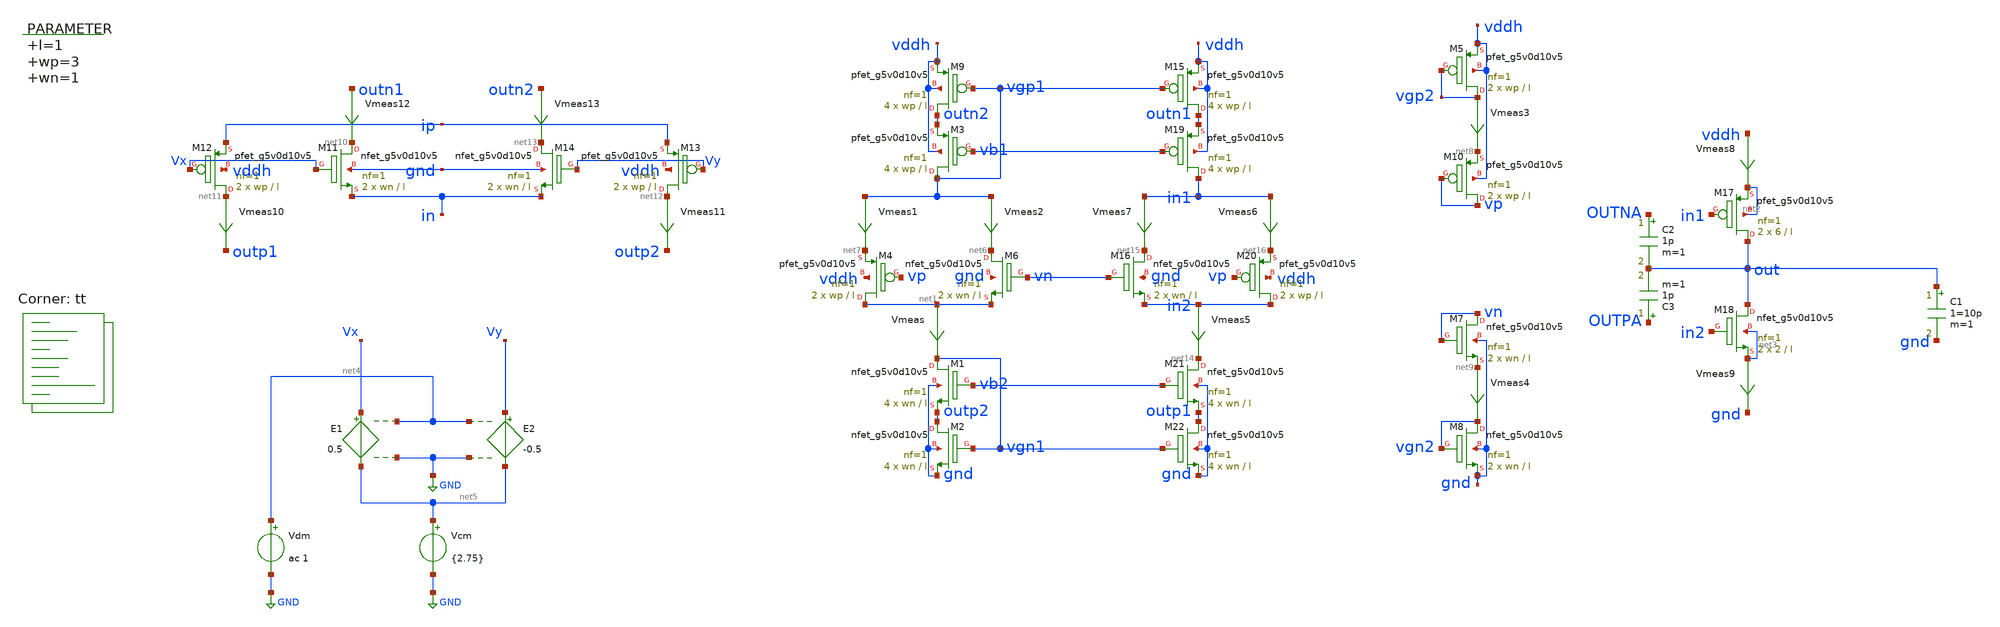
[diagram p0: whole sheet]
** sch_path: xschem/op_amp_output_stage.sch
**.subckt op_amp_output_stage
Vmeas net1 vgn1 0
.save i(vmeas)
XM9 outn2 vgp1 vddh vddh sky130_fd_pr__pfet_g5v0d10v5 L=l W=wp nf=1 ad='int((nf+1)/2) * W/nf * 0.29'
+ as='int((nf+2)/2) * W/nf * 0.29' pd='2*int((nf+1)/2) * (W/nf + 0.29)' ps='2*int((nf+2)/2) * (W/nf + 0.29)'
+ nrd='0.29 / W' nrs='0.29 / W' sa=0 sb=0 sd=0 mult=4 m=4
XM6 net6 vn net1 gnd sky130_fd_pr__nfet_g5v0d10v5 L=l W=wn nf=1 ad='int((nf+1)/2) * W/nf * 0.29' as='int((nf+2)/2) * W/nf * 0.29'
+ pd='2*int((nf+1)/2) * (W/nf + 0.29)' ps='2*int((nf+2)/2) * (W/nf + 0.29)' nrd='0.29 / W' nrs='0.29 / W'
+ sa=0 sb=0 sd=0 mult=2 m=2
Vmeas1 vgp1 net7 0
.save i(vmeas1)
Vmeas2 vgp1 net6 0
.save i(vmeas2)
Vmeas3 vgp2 net8 0
.save i(vmeas3)
Vmeas4 net9 vgn2 0
.save i(vmeas4)
XM3 vgp1 vb1 outn2 vddh sky130_fd_pr__pfet_g5v0d10v5 L=l W=wp nf=1 ad='int((nf+1)/2) * W/nf * 0.29' as='int((nf+2)/2) * W/nf * 0.29'
+ pd='2*int((nf+1)/2) * (W/nf + 0.29)' ps='2*int((nf+2)/2) * (W/nf + 0.29)' nrd='0.29 / W' nrs='0.29 / W'
+ sa=0 sb=0 sd=0 mult=4 m=4
XM4 net1 vp net7 vddh sky130_fd_pr__pfet_g5v0d10v5 L=l W=wp nf=1 ad='int((nf+1)/2) * W/nf * 0.29' as='int((nf+2)/2) * W/nf * 0.29'
+ pd='2*int((nf+1)/2) * (W/nf + 0.29)' ps='2*int((nf+2)/2) * (W/nf + 0.29)' nrd='0.29 / W' nrs='0.29 / W'
+ sa=0 sb=0 sd=0 mult=2 m=2
XM5 vgp2 vgp2 vddh vddh sky130_fd_pr__pfet_g5v0d10v5 L=l W=wp nf=1 ad='int((nf+1)/2) * W/nf * 0.29' as='int((nf+2)/2) * W/nf * 0.29'
+ pd='2*int((nf+1)/2) * (W/nf + 0.29)' ps='2*int((nf+2)/2) * (W/nf + 0.29)' nrd='0.29 / W' nrs='0.29 / W'
+ sa=0 sb=0 sd=0 mult=2 m=2
XM10 vp vp net8 vddh sky130_fd_pr__pfet_g5v0d10v5 L=l W=wp nf=1 ad='int((nf+1)/2) * W/nf * 0.29' as='int((nf+2)/2) * W/nf * 0.29'
+ pd='2*int((nf+1)/2) * (W/nf + 0.29)' ps='2*int((nf+2)/2) * (W/nf + 0.29)' nrd='0.29 / W' nrs='0.29 / W'
+ sa=0 sb=0 sd=0 mult=2 m=2
XM1 vgn1 vb2 outp2 gnd sky130_fd_pr__nfet_g5v0d10v5 L=l W=wn nf=1 ad='int((nf+1)/2) * W/nf * 0.29' as='int((nf+2)/2) * W/nf * 0.29'
+ pd='2*int((nf+1)/2) * (W/nf + 0.29)' ps='2*int((nf+2)/2) * (W/nf + 0.29)' nrd='0.29 / W' nrs='0.29 / W'
+ sa=0 sb=0 sd=0 mult=4 m=4
XM2 outp2 vgn1 gnd gnd sky130_fd_pr__nfet_g5v0d10v5 L=l W=wn nf=1 ad='int((nf+1)/2) * W/nf * 0.29' as='int((nf+2)/2) * W/nf * 0.29'
+ pd='2*int((nf+1)/2) * (W/nf + 0.29)' ps='2*int((nf+2)/2) * (W/nf + 0.29)' nrd='0.29 / W' nrs='0.29 / W'
+ sa=0 sb=0 sd=0 mult=4 m=4
XM7 vn vn net9 gnd sky130_fd_pr__nfet_g5v0d10v5 L=l W=wn nf=1 ad='int((nf+1)/2) * W/nf * 0.29' as='int((nf+2)/2) * W/nf * 0.29'
+ pd='2*int((nf+1)/2) * (W/nf + 0.29)' ps='2*int((nf+2)/2) * (W/nf + 0.29)' nrd='0.29 / W' nrs='0.29 / W'
+ sa=0 sb=0 sd=0 mult=2 m=2
XM8 vgn2 vgn2 gnd gnd sky130_fd_pr__nfet_g5v0d10v5 L=l W=wn nf=1 ad='int((nf+1)/2) * W/nf * 0.29' as='int((nf+2)/2) * W/nf * 0.29'
+ pd='2*int((nf+1)/2) * (W/nf + 0.29)' ps='2*int((nf+2)/2) * (W/nf + 0.29)' nrd='0.29 / W' nrs='0.29 / W'
+ sa=0 sb=0 sd=0 mult=2 m=2
.param l=1 wp=3 wn=1
XM17 out in1 net2 net2 sky130_fd_pr__pfet_g5v0d10v5 L=l W=6 nf=1 ad='int((nf+1)/2) * W/nf * 0.29' as='int((nf+2)/2) * W/nf * 0.29'
+ pd='2*int((nf+1)/2) * (W/nf + 0.29)' ps='2*int((nf+2)/2) * (W/nf + 0.29)' nrd='0.29 / W' nrs='0.29 / W'
+ sa=0 sb=0 sd=0 mult=2 m=2
XM18 out in2 net3 net3 sky130_fd_pr__nfet_g5v0d10v5 L=l W=2 nf=1 ad='int((nf+1)/2) * W/nf * 0.29' as='int((nf+2)/2) * W/nf * 0.29'
+ pd='2*int((nf+1)/2) * (W/nf + 0.29)' ps='2*int((nf+2)/2) * (W/nf + 0.29)' nrd='0.29 / W' nrs='0.29 / W'
+ sa=0 sb=0 sd=0 mult=2 m=2
Vmeas8 vddh net2 0
.save i(vmeas8)
Vmeas9 net3 gnd 0
.save i(vmeas9)
C1 out gnd 1=10p m=1
XM11 net10 Vx in gnd sky130_fd_pr__nfet_g5v0d10v5 L=l W=wn nf=1 ad='int((nf+1)/2) * W/nf * 0.29' as='int((nf+2)/2) * W/nf * 0.29'
+ pd='2*int((nf+1)/2) * (W/nf + 0.29)' ps='2*int((nf+2)/2) * (W/nf + 0.29)' nrd='0.29 / W' nrs='0.29 / W'
+ sa=0 sb=0 sd=0 mult=2 m=2
XM12 net11 Vx ip vddh sky130_fd_pr__pfet_g5v0d10v5 L=l W=wp nf=1 ad='int((nf+1)/2) * W/nf * 0.29' as='int((nf+2)/2) * W/nf * 0.29'
+ pd='2*int((nf+1)/2) * (W/nf + 0.29)' ps='2*int((nf+2)/2) * (W/nf + 0.29)' nrd='0.29 / W' nrs='0.29 / W'
+ sa=0 sb=0 sd=0 mult=2 m=2
XM13 net12 Vy ip vddh sky130_fd_pr__pfet_g5v0d10v5 L=l W=wp nf=1 ad='int((nf+1)/2) * W/nf * 0.29' as='int((nf+2)/2) * W/nf * 0.29'
+ pd='2*int((nf+1)/2) * (W/nf + 0.29)' ps='2*int((nf+2)/2) * (W/nf + 0.29)' nrd='0.29 / W' nrs='0.29 / W'
+ sa=0 sb=0 sd=0 mult=2 m=2
XM14 net13 Vy in gnd sky130_fd_pr__nfet_g5v0d10v5 L=l W=wn nf=1 ad='int((nf+1)/2) * W/nf * 0.29' as='int((nf+2)/2) * W/nf * 0.29'
+ pd='2*int((nf+1)/2) * (W/nf + 0.29)' ps='2*int((nf+2)/2) * (W/nf + 0.29)' nrd='0.29 / W' nrs='0.29 / W'
+ sa=0 sb=0 sd=0 mult=2 m=2
Vmeas5 in2 net14 0
.save i(vmeas5)
XM15 outn1 vgp1 vddh vddh sky130_fd_pr__pfet_g5v0d10v5 L=l W=wp nf=1 ad='int((nf+1)/2) * W/nf * 0.29'
+ as='int((nf+2)/2) * W/nf * 0.29' pd='2*int((nf+1)/2) * (W/nf + 0.29)' ps='2*int((nf+2)/2) * (W/nf + 0.29)'
+ nrd='0.29 / W' nrs='0.29 / W' sa=0 sb=0 sd=0 mult=4 m=4
XM16 net15 vn in2 gnd sky130_fd_pr__nfet_g5v0d10v5 L=l W=wn nf=1 ad='int((nf+1)/2) * W/nf * 0.29' as='int((nf+2)/2) * W/nf * 0.29'
+ pd='2*int((nf+1)/2) * (W/nf + 0.29)' ps='2*int((nf+2)/2) * (W/nf + 0.29)' nrd='0.29 / W' nrs='0.29 / W'
+ sa=0 sb=0 sd=0 mult=2 m=2
Vmeas6 in1 net16 0
.save i(vmeas6)
Vmeas7 in1 net15 0
.save i(vmeas7)
XM19 in1 vb1 outn1 vddh sky130_fd_pr__pfet_g5v0d10v5 L=l W=wp nf=1 ad='int((nf+1)/2) * W/nf * 0.29' as='int((nf+2)/2) * W/nf * 0.29'
+ pd='2*int((nf+1)/2) * (W/nf + 0.29)' ps='2*int((nf+2)/2) * (W/nf + 0.29)' nrd='0.29 / W' nrs='0.29 / W'
+ sa=0 sb=0 sd=0 mult=4 m=4
XM20 in2 vp net16 vddh sky130_fd_pr__pfet_g5v0d10v5 L=l W=wp nf=1 ad='int((nf+1)/2) * W/nf * 0.29' as='int((nf+2)/2) * W/nf * 0.29'
+ pd='2*int((nf+1)/2) * (W/nf + 0.29)' ps='2*int((nf+2)/2) * (W/nf + 0.29)' nrd='0.29 / W' nrs='0.29 / W'
+ sa=0 sb=0 sd=0 mult=2 m=2
XM21 net14 vb2 outp1 gnd sky130_fd_pr__nfet_g5v0d10v5 L=l W=wn nf=1 ad='int((nf+1)/2) * W/nf * 0.29'
+ as='int((nf+2)/2) * W/nf * 0.29' pd='2*int((nf+1)/2) * (W/nf + 0.29)' ps='2*int((nf+2)/2) * (W/nf + 0.29)'
+ nrd='0.29 / W' nrs='0.29 / W' sa=0 sb=0 sd=0 mult=4 m=4
XM22 outp1 vgn1 gnd gnd sky130_fd_pr__nfet_g5v0d10v5 L=l W=wn nf=1 ad='int((nf+1)/2) * W/nf * 0.29' as='int((nf+2)/2) * W/nf * 0.29'
+ pd='2*int((nf+1)/2) * (W/nf + 0.29)' ps='2*int((nf+2)/2) * (W/nf + 0.29)' nrd='0.29 / W' nrs='0.29 / W'
+ sa=0 sb=0 sd=0 mult=4 m=4
Vmeas10 net11 outp1 0
.save i(vmeas10)
Vmeas11 net12 outp2 0
.save i(vmeas11)
Vmeas12 outn1 net10 0
.save i(vmeas12)
Vmeas13 outn2 net13 0
.save i(vmeas13)
E1 Vx net5 net4 GND 0.5
E2 Vy net5 net4 GND -0.5
Vdm net4 GND ac 1
Vcm net5 GND {2.75}
C2 OUTNA out 1p m=1
C3 OUTPA out 1p m=1
**** begin user architecture code
.lib $::SKYWATER_MODELS/sky130.lib.spice tt



  .option wnflag=1
  .option safecurrents
  ********************Static Current Sources***************************
  Ivp vp gnd 5u
  Ivn vddh vn 5u
  Iip vddh ip 1u
  Iin in gnd 1u
  ********************Static Voltage Sources***************************
  Vddh vddh gnd dc 5.5

  vb1 vb1 gnd dc 3.37
  vb2 vb2 gnd dc 1.95
  ********************Dynamic Voltage Sources***************************
  *******Calculation**********
  .param base_f=100e3 base_t={1/base_f} base_th={base_t/2} base_d={base_th}
  .param d2_th ={base_th} d2_t={2*d2_th}
  .param d1_th ={4*d2_th} d1_t={d0_th}
  .param d0_th ={4*d1_th} d0_t={4*d0_th}

  .param d20_d ={0} d21_d={1*d2_th} d22_d={2*d2_th} d23_d={3*d2_th}
  .param d10_d ={0} d11_d={1*d1_th} d12_d={2*d1_th} d13_d={3*d1_th}
  .param d00_d ={0} d01_d={1*d0_th} d02_d={2*d0_th} d03_d={3*d0_th}
  *******Signals**********
  .param vhi=5.5
*  Vin1 b[0] gnd pulse(0 {vhi} {0} 1p 1p {10u} {20u})
*  Vin2 b[1] gnd pulse(0 {vhi} {0} 1p 1p {20u} {40u})
  vin1 inx gnd sin({5.5/2} {5.5/2} 100k)
*  vin2 iny gnd sin({5.5/2} {-5.5/2} 100k)
  ********************Simulation Commands*****************************
  .control
     reset
     save all
     *dc vin 0 5.5 0.001
     *dc Iy 0 1u 0.001u
     *tran 1n 50u
     ac dec 100 1 10MEG
     write output_stage-tb.raw
     set appendwrite
*    quit 0
  .endc



**** end user architecture code
**.ends
.GLOBAL GND
.end
